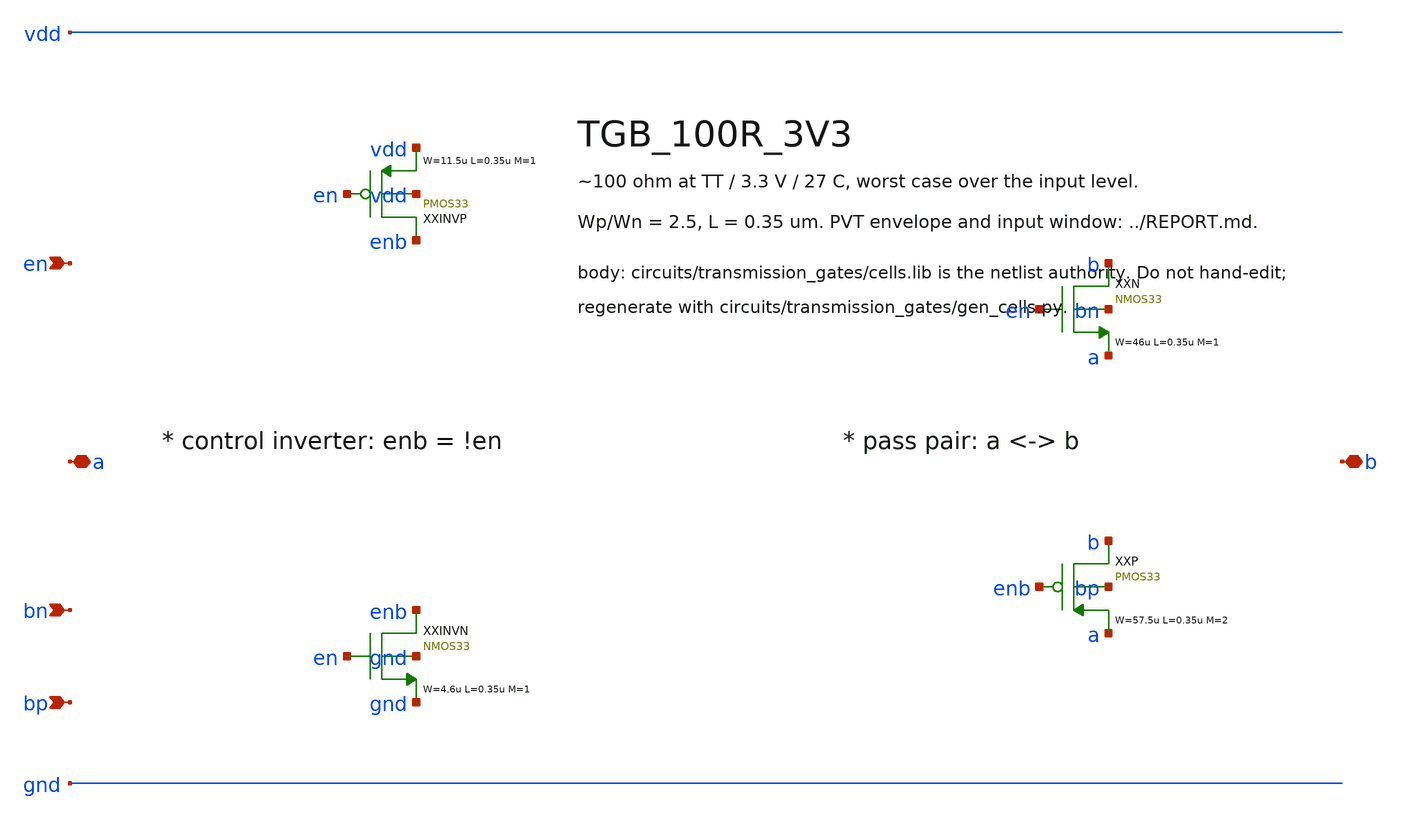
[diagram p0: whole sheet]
** sch_path: xschem/transmission_gates/TGB_100R_3V3.sch
**.subckt TGB_100R_3V3 a b en bn bp
*.iopin a
*.iopin b
*.ipin en
*.ipin bn
*.ipin bp
XXINVP enb en vdd vdd PMOS33 W=11.5u L=0.35u M=1 MM_SIGMA=0
XXINVN enb en gnd gnd NMOS33 W=4.6u L=0.35u M=1 MM_SIGMA=0
XXN b en a bn NMOS33 W=46u L=0.35u M=1 MM_SIGMA=0
XXP b enb a bp PMOS33 W=57.5u L=0.35u M=2 MM_SIGMA=0
**.ends
.end
